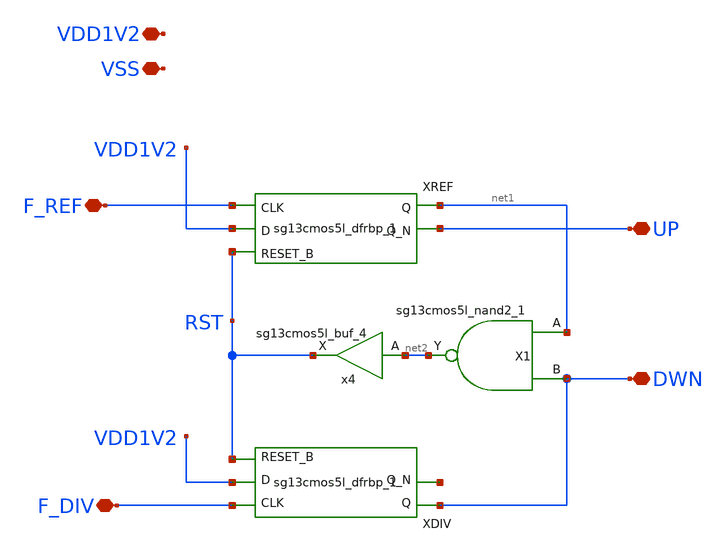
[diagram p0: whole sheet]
** sch_path: macros/pll_top/schematic/xschem/pfd_top.sch
* Copyright (C) 1998-2024 Stefan Frederik Schippers
* This program is free software; you can redistribute it and/or modify
* it under the terms of the GNU General Public License as published by
* the Free Software Foundation; either version 2 of the License, or
* (at your option) any later version.
* This program is distributed in the hope that it will be useful,
* but WITHOUT ANY WARRANTY; without even the implied warranty of
* MERCHANTABILITY or FITNESS FOR A PARTICULAR PURPOSE.  See the
* GNU General Public License for more details.
* You should have received a copy of the GNU General Public License
* along with this program; if not, write to the Free Software
**.subckt pfd_top F_DIV F_REF UP DWN VDD1V2 VSS
*.iopin F_DIV
*.iopin F_REF
*.iopin UP
*.iopin DWN
*.iopin VDD1V2
*.iopin VSS
X1 net2 net1 DWN VDD1V2 VSS sg13cmos5l_nand2_1
XREF net1 UP F_REF VDD1V2 RST VDD1V2 VSS sg13cmos5l_dfrbp_1
XDIV DWN net3 F_DIV VDD1V2 RST VDD1V2 VSS sg13cmos5l_dfrbp_1
x4 RST net2 VDD1V2 VSS sg13cmos5l_buf_4
**.ends
.end
